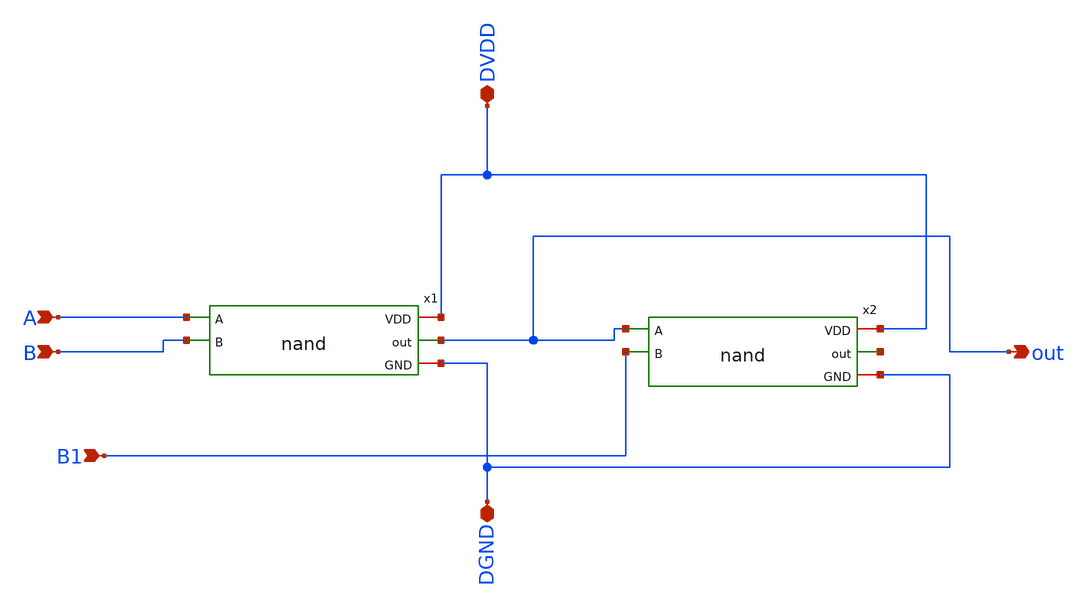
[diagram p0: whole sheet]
** sch_path: assignments/assignment5/nand_tb.sch
**.subckt nand_tb A out DGND DVDD B B1
*.ipin A
*.opin out
*.iopin DGND
*.iopin DVDD
*.ipin B
*.ipin B1
x1 DVDD A out B DGND nand
x2 DVDD out net1 B1 DGND nand
**.ends

* expanding   symbol:  nand.sym # of pins=5
** sym_path: assignments/assignment5/nand.sym
** sch_path: assignments/assignment5/nand.sch
.subckt nand VDD A out B GND
*.ipin A
*.opin out
*.iopin VDD
*.iopin GND
*.ipin B
XM1 out A net1 GND sky130_fd_pr__nfet_01v8 L=0.15 W=1.68 nf=4 ad='int((nf+1)/2) * W/nf * 0.29' as='int((nf+2)/2) * W/nf * 0.29'
+ pd='2*int((nf+1)/2) * (W/nf + 0.29)' ps='2*int((nf+2)/2) * (W/nf + 0.29)' nrd='0.29 / W' nrs='0.29 / W'
+ sa=0 sb=0 sd=0 mult=1 m=1
XM2 out A VDD VDD sky130_fd_pr__pfet_01v8 L=0.15 W=1.68 nf=4 ad='int((nf+1)/2) * W/nf * 0.29' as='int((nf+2)/2) * W/nf * 0.29'
+ pd='2*int((nf+1)/2) * (W/nf + 0.29)' ps='2*int((nf+2)/2) * (W/nf + 0.29)' nrd='0.29 / W' nrs='0.29 / W'
+ sa=0 sb=0 sd=0 mult=1 m=1
XM3 net1 B GND GND sky130_fd_pr__nfet_01v8 L=0.15 W=1.68 nf=4 ad='int((nf+1)/2) * W/nf * 0.29' as='int((nf+2)/2) * W/nf * 0.29'
+ pd='2*int((nf+1)/2) * (W/nf + 0.29)' ps='2*int((nf+2)/2) * (W/nf + 0.29)' nrd='0.29 / W' nrs='0.29 / W'
+ sa=0 sb=0 sd=0 mult=1 m=1
XM4 out B VDD VDD sky130_fd_pr__pfet_01v8 L=0.15 W=1.68 nf=4 ad='int((nf+1)/2) * W/nf * 0.29' as='int((nf+2)/2) * W/nf * 0.29'
+ pd='2*int((nf+1)/2) * (W/nf + 0.29)' ps='2*int((nf+2)/2) * (W/nf + 0.29)' nrd='0.29 / W' nrs='0.29 / W'
+ sa=0 sb=0 sd=0 mult=1 m=1
.ends

.end
